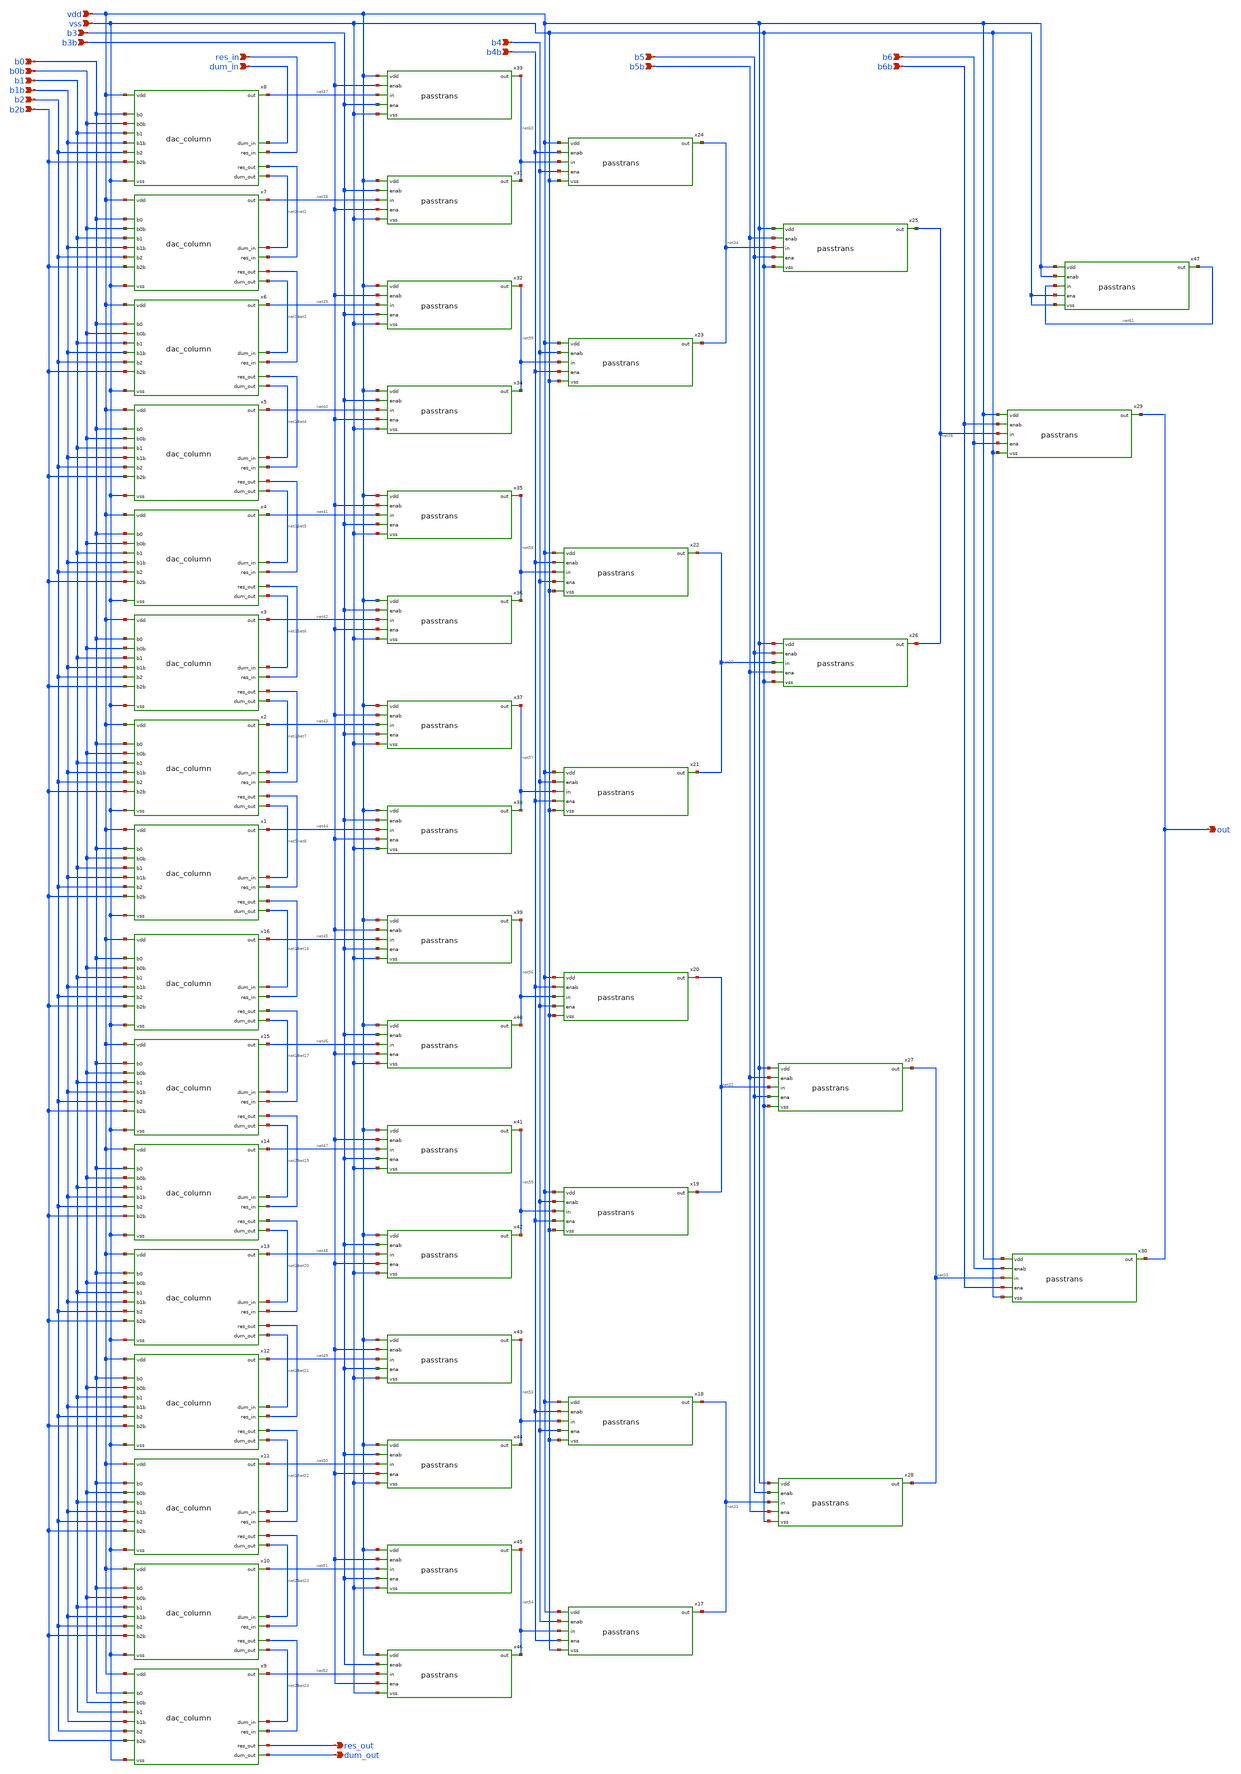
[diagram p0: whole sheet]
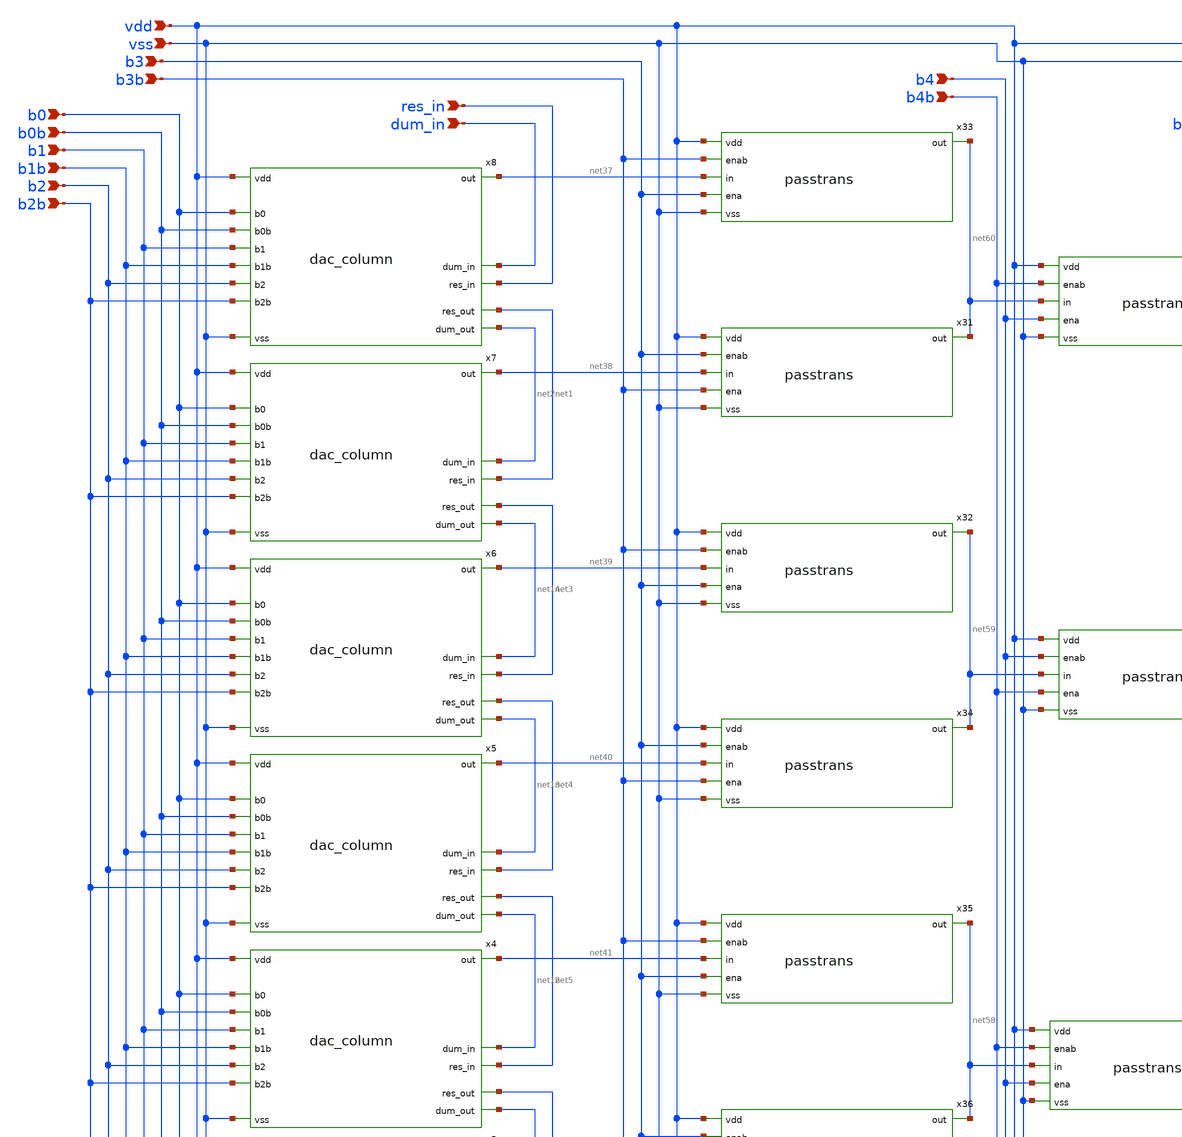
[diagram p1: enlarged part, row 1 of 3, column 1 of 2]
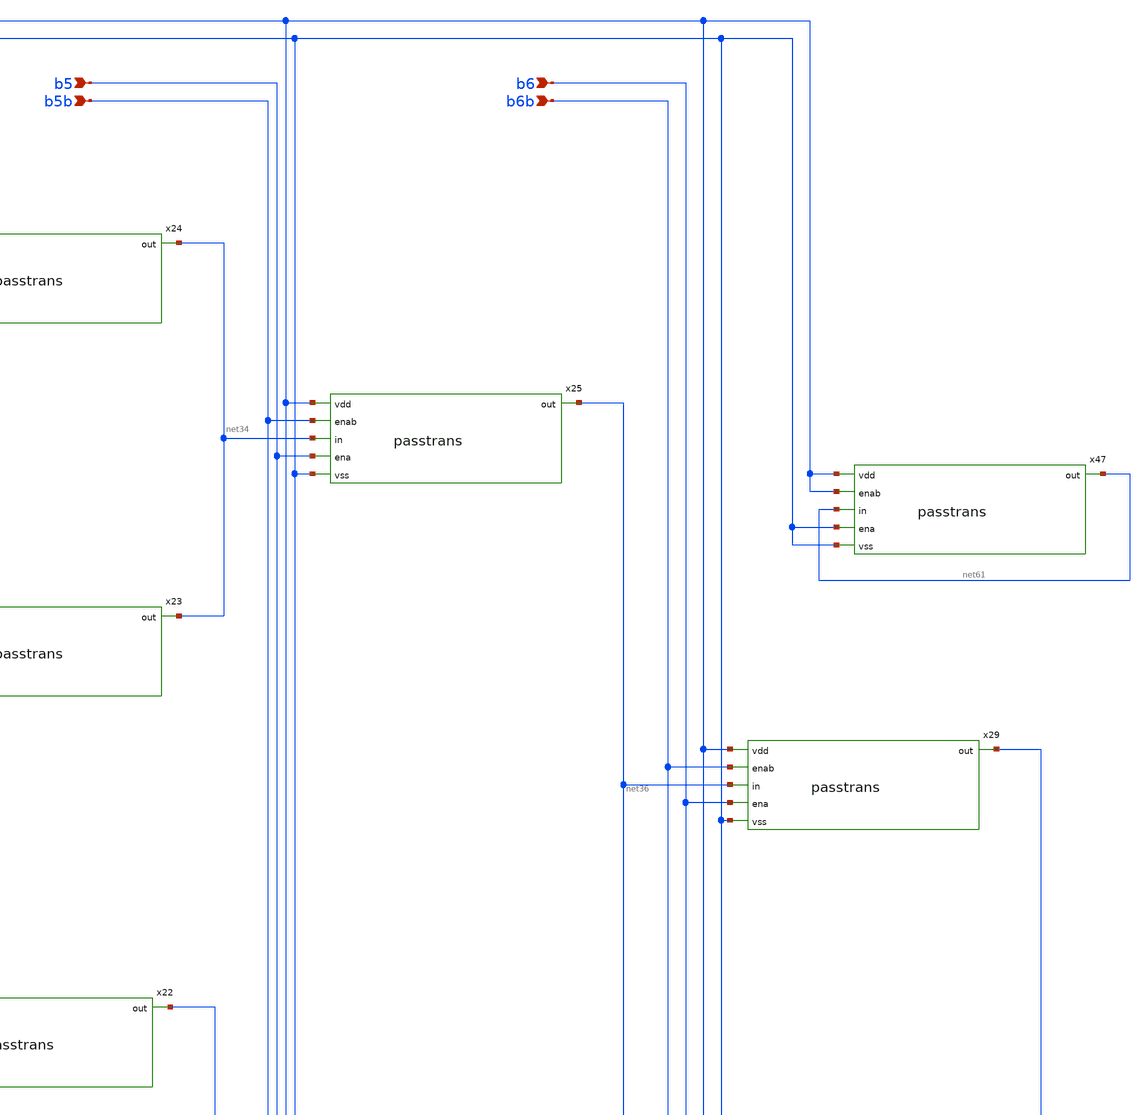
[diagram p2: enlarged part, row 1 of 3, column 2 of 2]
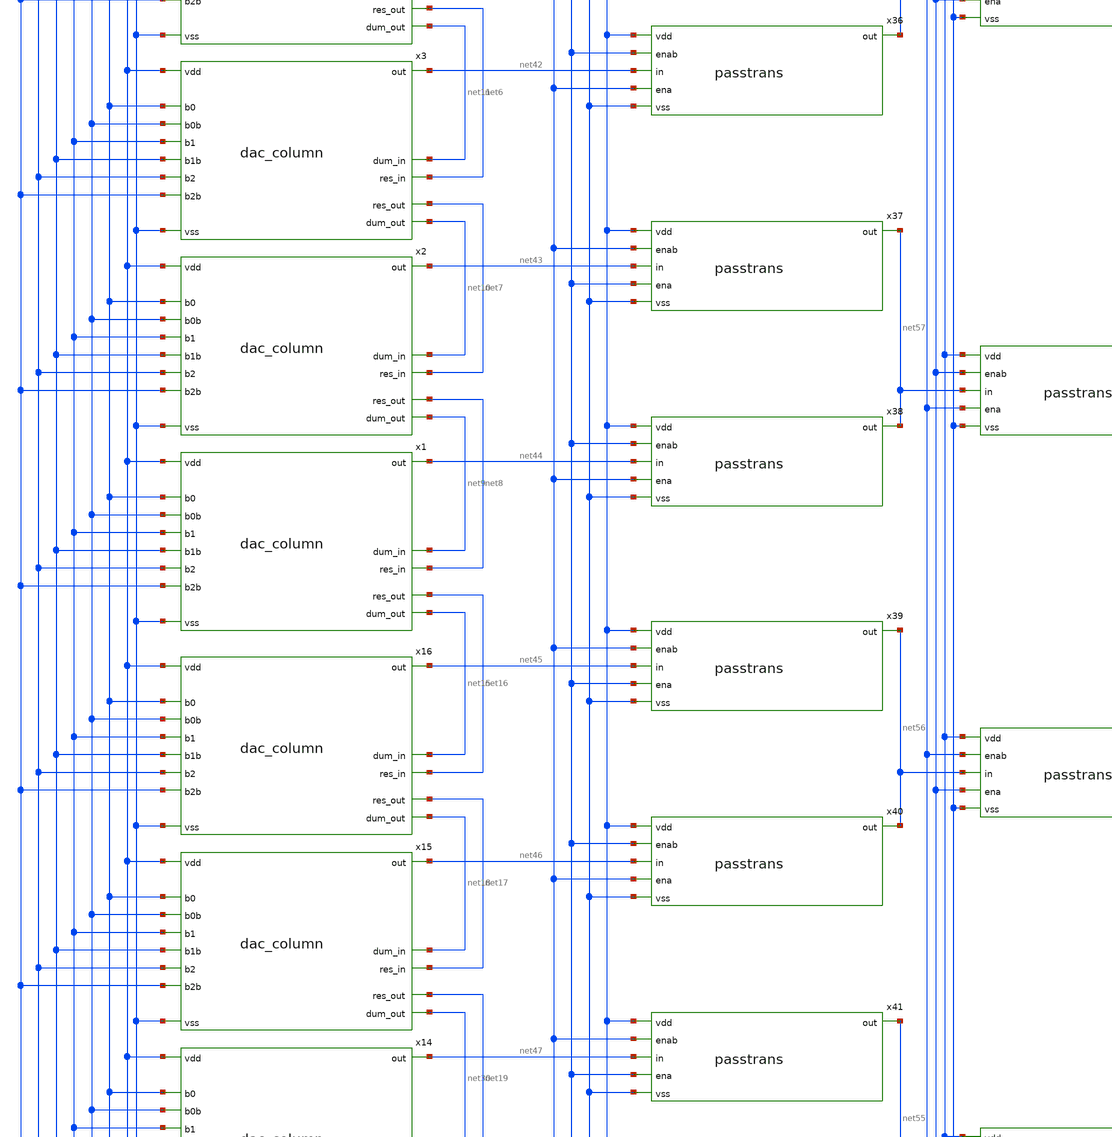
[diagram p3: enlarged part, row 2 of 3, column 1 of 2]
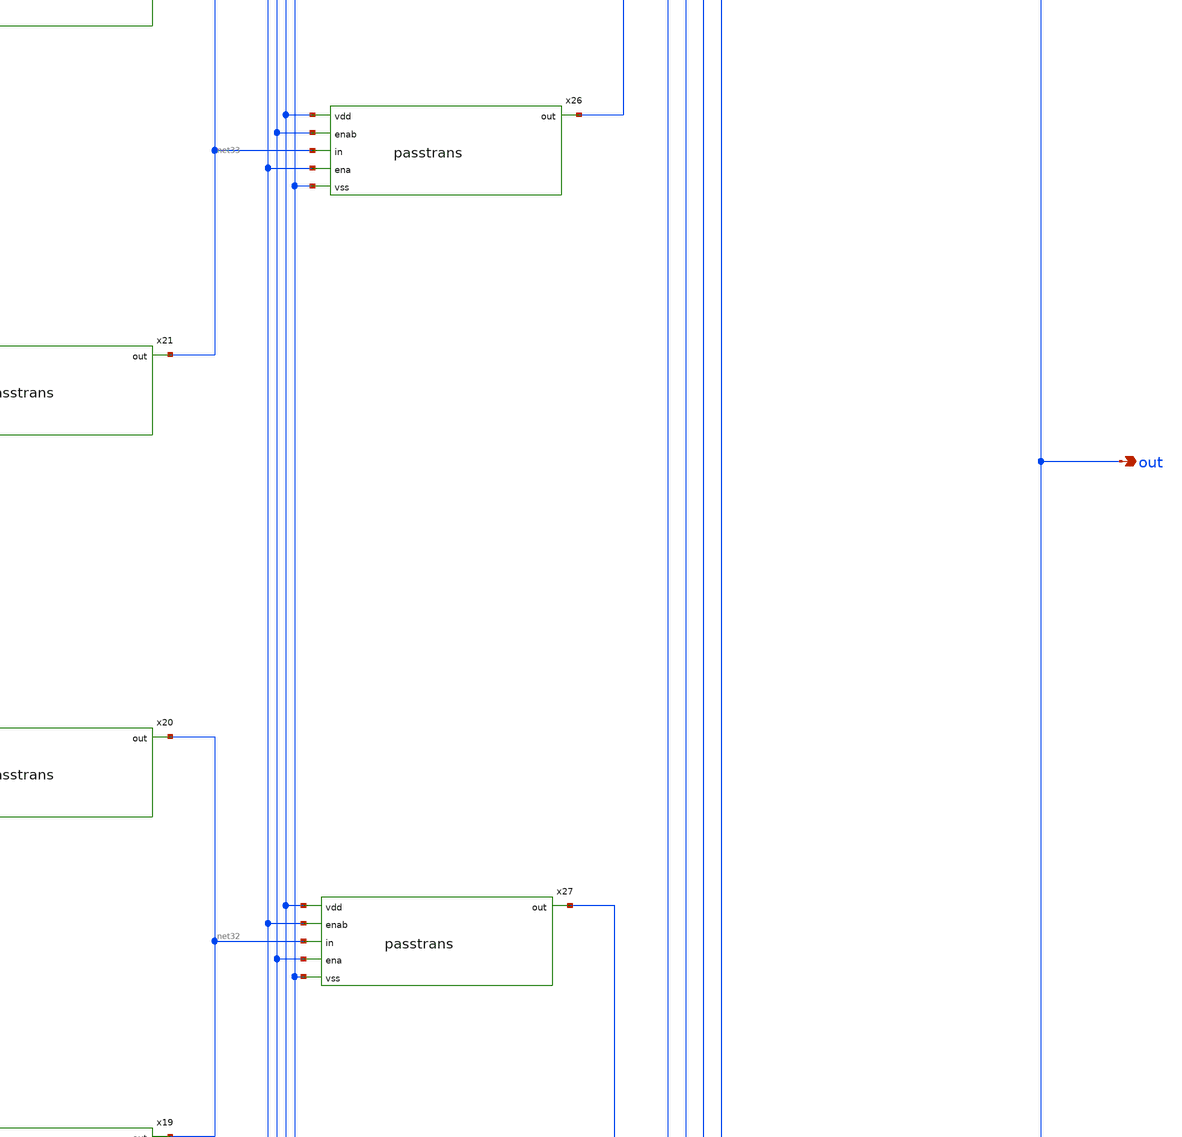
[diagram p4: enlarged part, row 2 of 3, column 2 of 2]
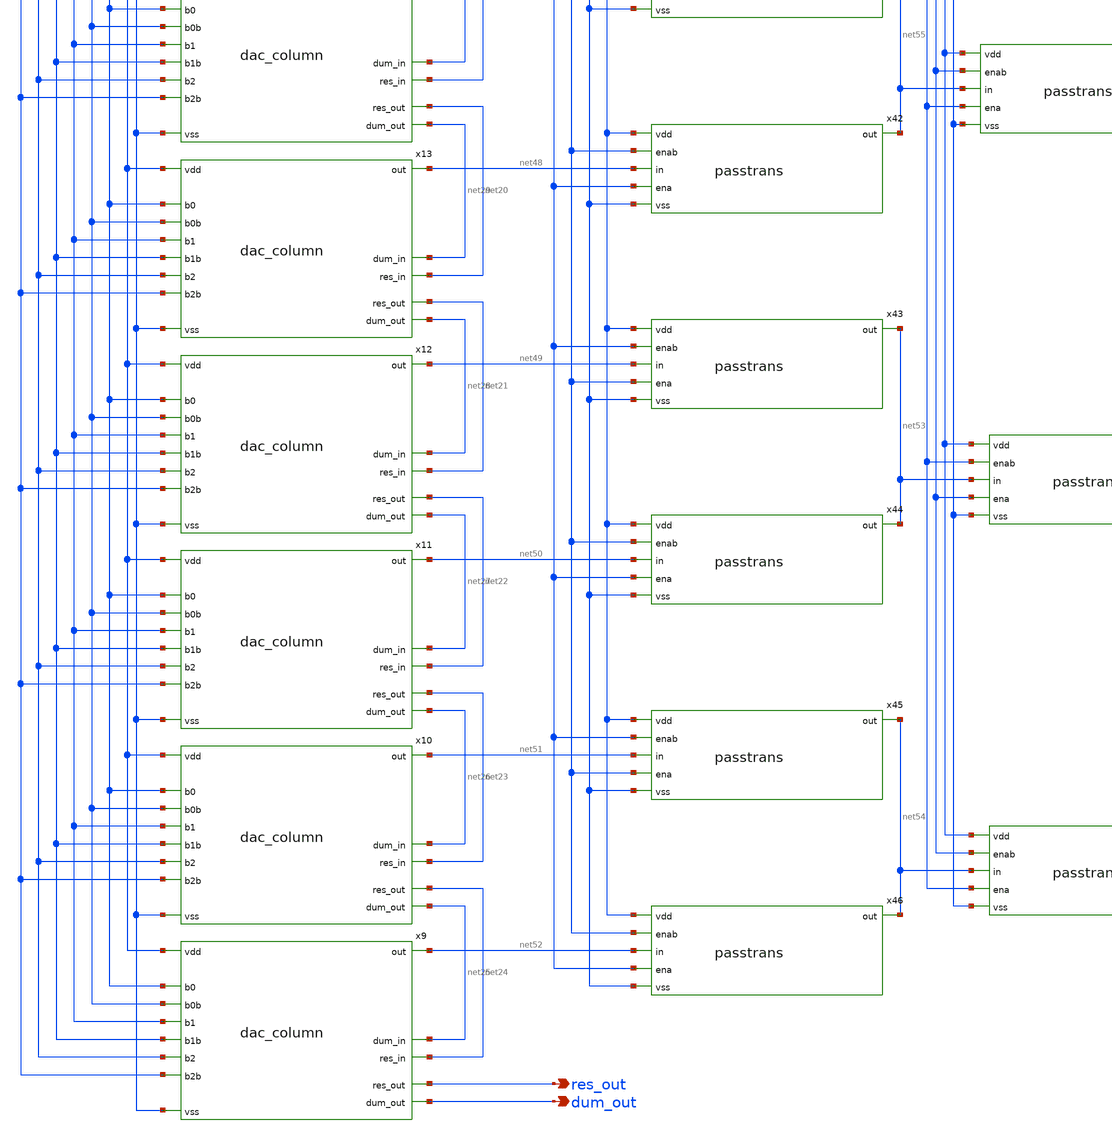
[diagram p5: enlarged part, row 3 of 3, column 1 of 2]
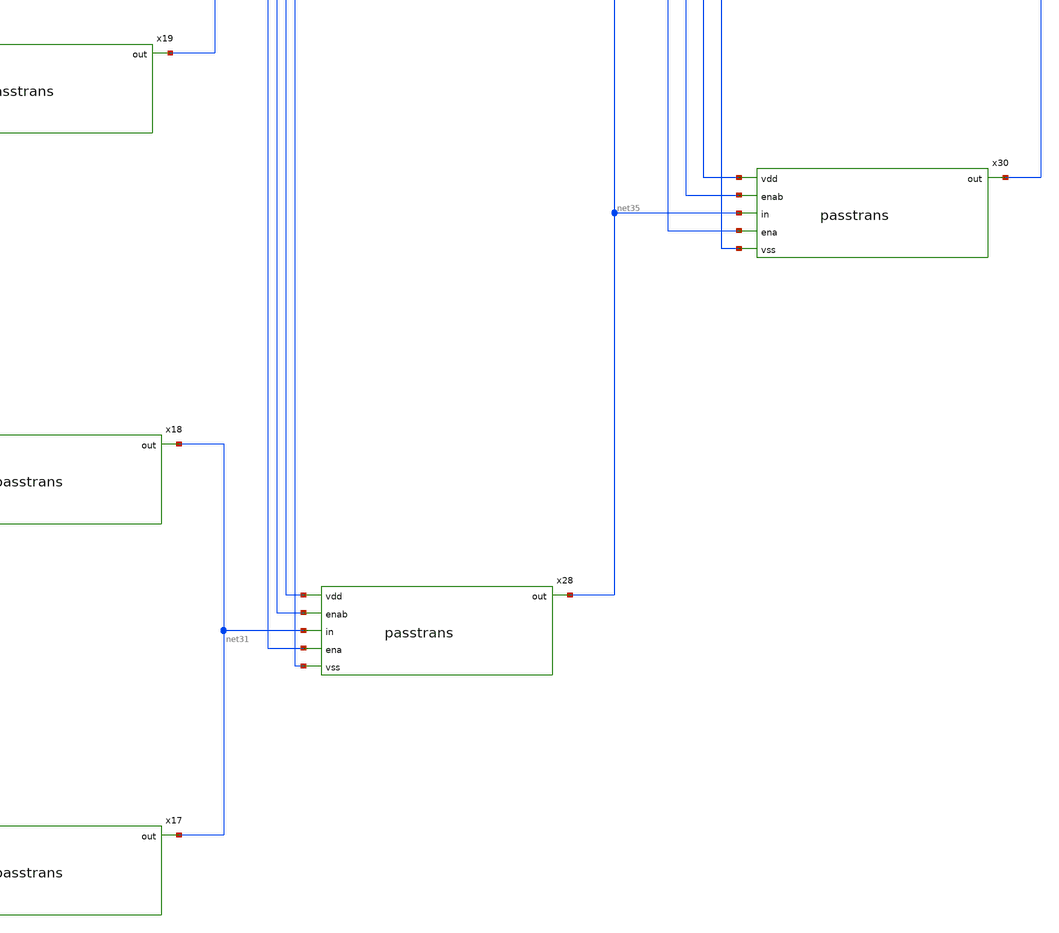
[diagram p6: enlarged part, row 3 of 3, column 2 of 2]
** sch_path: xschem/dac_half.sch
**.subckt dac_half res_in res_out out vdd vss b3 b3b b5 b5b b6 b6b dum_out dum_in b4 b4b b0 b0b b1
*+ b1b b2 b2b
*.ipin res_in
*.opin res_out
*.opin out
*.ipin vdd
*.ipin vss
*.ipin b3
*.ipin b3b
*.ipin b5
*.ipin b5b
*.ipin b6
*.ipin b6b
*.opin dum_out
*.ipin dum_in
*.ipin b4
*.ipin b4b
*.ipin b0
*.ipin b0b
*.ipin b1
*.ipin b1b
*.ipin b2
*.ipin b2b
x1 b2 b2b b1 b1b b0 b0b vdd net9 net8 net44 net16 vss net15 dac_column
x2 b2 b2b b1 b1b b0 b0b vdd net10 net7 net43 net8 vss net9 dac_column
x3 b2 b2b b1 b1b b0 b0b vdd net11 net6 net42 net7 vss net10 dac_column
x4 b2 b2b b1 b1b b0 b0b vdd net12 net5 net41 net6 vss net11 dac_column
x5 b2 b2b b1 b1b b0 b0b vdd net13 net4 net40 net5 vss net12 dac_column
x6 b2 b2b b1 b1b b0 b0b vdd net14 net3 net39 net4 vss net13 dac_column
x7 b2 b2b b1 b1b b0 b0b vdd net2 net1 net38 net3 vss net14 dac_column
x8 b2 b2b b1 b1b b0 b0b vdd dum_in res_in net37 net1 vss net2 dac_column
x9 b2 b2b b1 b1b b0 b0b vdd net25 net24 net52 res_out vss dum_out dac_column
x10 b2 b2b b1 b1b b0 b0b vdd net26 net23 net51 net24 vss net25 dac_column
x11 b2 b2b b1 b1b b0 b0b vdd net27 net22 net50 net23 vss net26 dac_column
x12 b2 b2b b1 b1b b0 b0b vdd net28 net21 net49 net22 vss net27 dac_column
x13 b2 b2b b1 b1b b0 b0b vdd net29 net20 net48 net21 vss net28 dac_column
x14 b2 b2b b1 b1b b0 b0b vdd net30 net19 net47 net20 vss net29 dac_column
x15 b2 b2b b1 b1b b0 b0b vdd net18 net17 net46 net19 vss net30 dac_column
x16 b2 b2b b1 b1b b0 b0b vdd net15 net16 net45 net17 vss net18 dac_column
x17 vdd b4 net31 net54 b4b vss passtrans
x18 vdd b4b net31 net53 b4 vss passtrans
x19 vdd b4 net32 net55 b4b vss passtrans
x20 vdd b4b net32 net56 b4 vss passtrans
x21 vdd b4 net33 net57 b4b vss passtrans
x22 vdd b4b net33 net58 b4 vss passtrans
x23 vdd b4 net34 net59 b4b vss passtrans
x24 vdd b4b net34 net60 b4 vss passtrans
x25 vdd b5b net36 net34 b5 vss passtrans
x26 vdd b5 net36 net33 b5b vss passtrans
x27 vdd b5b net35 net32 b5 vss passtrans
x28 vdd b5 net35 net31 b5b vss passtrans
x29 vdd b6b out net36 b6 vss passtrans
x30 vdd b6 out net35 b6b vss passtrans
x33 vdd b3b net60 net37 b3 vss passtrans
x31 vdd b3 net60 net38 b3b vss passtrans
x32 vdd b3b net59 net39 b3 vss passtrans
x34 vdd b3 net59 net40 b3b vss passtrans
x35 vdd b3b net58 net41 b3 vss passtrans
x36 vdd b3 net58 net42 b3b vss passtrans
x37 vdd b3b net57 net43 b3 vss passtrans
x38 vdd b3 net57 net44 b3b vss passtrans
x39 vdd b3b net56 net45 b3 vss passtrans
x40 vdd b3 net56 net46 b3b vss passtrans
x41 vdd b3b net55 net47 b3 vss passtrans
x42 vdd b3 net55 net48 b3b vss passtrans
x43 vdd b3b net53 net49 b3 vss passtrans
x44 vdd b3 net53 net50 b3b vss passtrans
x45 vdd b3b net54 net51 b3 vss passtrans
x46 vdd b3 net54 net52 b3b vss passtrans
x47 vdd vdd net61 net61 vss vss passtrans
**.ends
.end
